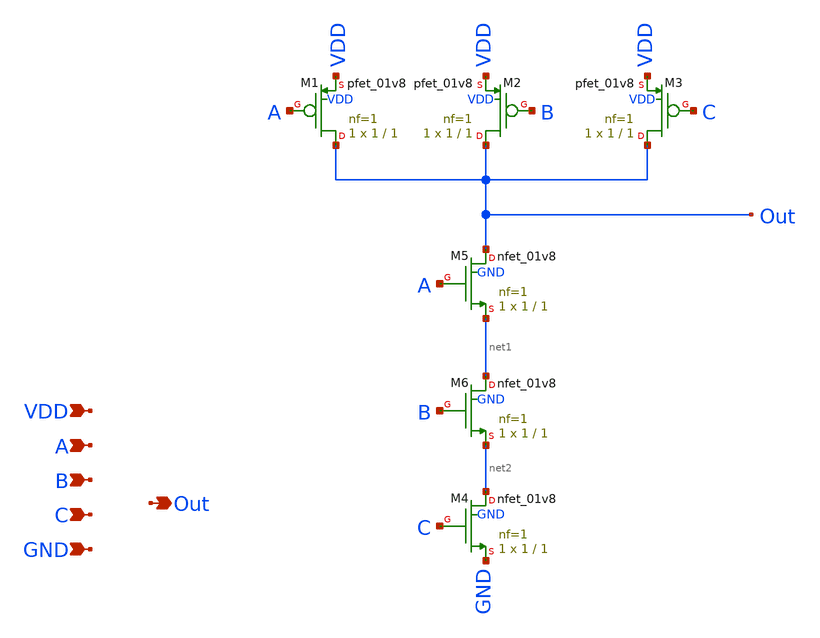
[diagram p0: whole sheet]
** sch_path: src/NAND3.sch
**.subckt NAND3 Out A B VDD GND C
*.opin Out
*.ipin A
*.ipin B
*.ipin VDD
*.ipin GND
*.ipin C
XM1 Out A VDD VDD sky130_fd_pr__pfet_01v8 L=1 W=1 nf=1 ad='int((1 + 1)/2) * 1 / 1 * 0.29' as='int((1 + 2)/2) * 1 / 1 * 0.29'
+ pd='2*int((1 + 1)/2) * (1 / 1 + 0.29)' ps='2*int((1 + 2)/2) * (1 / 1 + 0.29)' nrd='0.29 / 1 ' nrs='0.29 / 1 '
+ sa=0 sb=0 sd=0 mult=1 m=1
XM3 Out C VDD VDD sky130_fd_pr__pfet_01v8 L=1 W=1 nf=1 ad='int((1 + 1)/2) * 1 / 1 * 0.29' as='int((1 + 2)/2) * 1 / 1 * 0.29'
+ pd='2*int((1 + 1)/2) * (1 / 1 + 0.29)' ps='2*int((1 + 2)/2) * (1 / 1 + 0.29)' nrd='0.29 / 1 ' nrs='0.29 / 1 '
+ sa=0 sb=0 sd=0 mult=1 m=1
XM4 net2 C GND GND sky130_fd_pr__nfet_01v8 L=1 W=1 nf=1 ad='int((1 + 1)/2) * 1 / 1 * 0.29' as='int((1 + 2)/2) * 1 / 1 * 0.29'
+ pd='2*int((1 + 1)/2) * (1 / 1 + 0.29)' ps='2*int((1 + 2)/2) * (1 / 1 + 0.29)' nrd='0.29 / 1 ' nrs='0.29 / 1 '
+ sa=0 sb=0 sd=0 mult=1 m=1
XM5 Out A net1 GND sky130_fd_pr__nfet_01v8 L=1 W=1 nf=1 ad='int((1 + 1)/2) * 1 / 1 * 0.29' as='int((1 + 2)/2) * 1 / 1 * 0.29'
+ pd='2*int((1 + 1)/2) * (1 / 1 + 0.29)' ps='2*int((1 + 2)/2) * (1 / 1 + 0.29)' nrd='0.29 / 1 ' nrs='0.29 / 1 '
+ sa=0 sb=0 sd=0 mult=1 m=1
XM2 Out B VDD VDD sky130_fd_pr__pfet_01v8 L=1 W=1 nf=1 ad='int((1 + 1)/2) * 1 / 1 * 0.29' as='int((1 + 2)/2) * 1 / 1 * 0.29'
+ pd='2*int((1 + 1)/2) * (1 / 1 + 0.29)' ps='2*int((1 + 2)/2) * (1 / 1 + 0.29)' nrd='0.29 / 1 ' nrs='0.29 / 1 '
+ sa=0 sb=0 sd=0 mult=1 m=1
XM6 net1 B net2 GND sky130_fd_pr__nfet_01v8 L=1 W=1 nf=1 ad='int((1 + 1)/2) * 1 / 1 * 0.29' as='int((1 + 2)/2) * 1 / 1 * 0.29'
+ pd='2*int((1 + 1)/2) * (1 / 1 + 0.29)' ps='2*int((1 + 2)/2) * (1 / 1 + 0.29)' nrd='0.29 / 1 ' nrs='0.29 / 1 '
+ sa=0 sb=0 sd=0 mult=1 m=1
**** begin user architecture code

** opencircuitdesign pdks install
.lib $::SKYWATER_MODELS/sky130.lib.spice tt


**** end user architecture code
**.ends
.end
